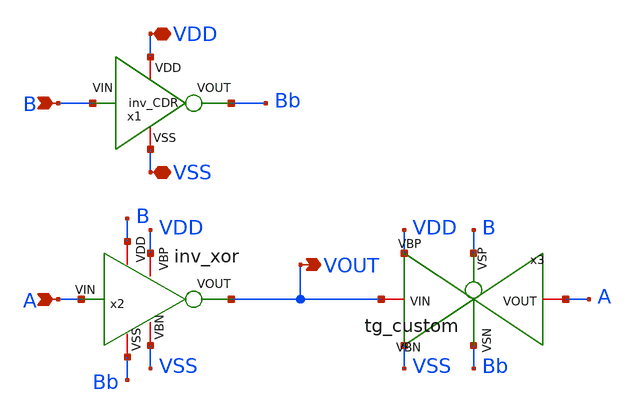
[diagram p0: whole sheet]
** sch_path: CDR4176-main/schematic/xschem/xor_custom/xor_custom.sch
**.subckt xor_custom A B VOUT VDD VSS
*.ipin A
*.ipin B
*.opin VOUT
*.iopin VDD
*.iopin VSS
x1 VDD Bb B VSS inv_CDR
x3 A Bb B VOUT VDD VSS tg_custom
x2 B VDD A VSS Bb VOUT inv_xor
**.ends

* expanding   symbol:  inv_CDR/inv_CDR.sym # of pins=4
** sym_path: CDR4176-main/schematic/xschem/inv_CDR/inv_CDR.sym
** sch_path: CDR4176-main/schematic/xschem/inv_CDR/inv_CDR.sch
.subckt inv_CDR VDD VOUT VIN VSS
*.iopin VDD
*.iopin VSS
*.opin VOUT
*.ipin VIN
XM2 VOUT VIN VDD VDD sg13_lv_pmos w=0.15u l=0.13u ng=1 m=1 mm_ok=1
XM1 VOUT VIN VSS VSS sg13_lv_nmos w=0.15u l=0.13u ng=1 m=1 mm_ok=1
.ends


* expanding   symbol:  tg_custom/tg_custom.sym # of pins=6
** sym_path: CDR4176-main/schematic/xschem/tg_custom/tg_custom.sym
** sch_path: CDR4176-main/schematic/xschem/tg_custom/tg_custom.sch
.subckt tg_custom VOUT VSN VSP VIN VBP VBN
*.iopin VIN
*.iopin VSN
*.iopin VOUT
*.iopin VSP
*.iopin VBN
*.iopin VBP
XM1 VOUT VSN VIN VBN sg13_lv_nmos w=0.15u l=0.13u ng=1 m=1 mm_ok=1
XM2 VOUT VSP VIN VBP sg13_lv_pmos w=0.3u l=0.13u ng=2 m=1 mm_ok=1
.ends


* expanding   symbol:  inv_xor/inv_xor.sym # of pins=6
** sym_path: CDR4176-main/schematic/xschem/inv_xor/inv_xor.sym
** sch_path: CDR4176-main/schematic/xschem/inv_xor/inv_xor.sch
.subckt inv_xor VDD VBP VIN VBN VSS VOUT
*.iopin VDD
*.iopin VSS
*.opin VOUT
*.ipin VIN
*.iopin VBP
*.iopin VBN
XM2 VOUT VIN VDD VBP sg13_lv_pmos w=0.15u l=0.13u ng=1 m=1 mm_ok=1
XM1 VOUT VIN VSS VBN sg13_lv_nmos w=0.15u l=0.13u ng=1 m=1 mm_ok=1
.ends

.end
